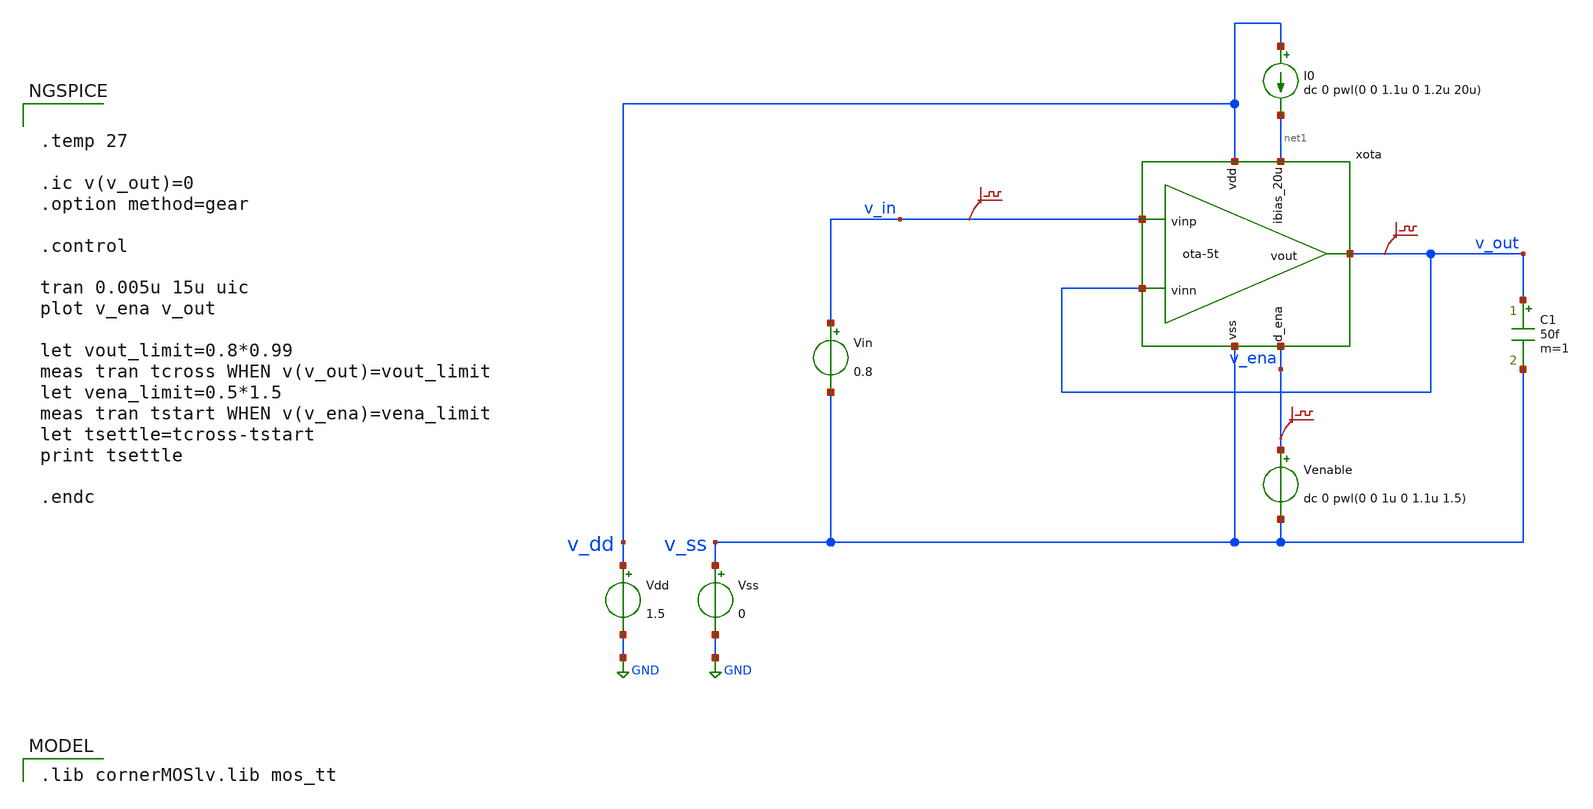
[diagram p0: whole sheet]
** sch_path: xschem/ota-5t_tb-tran.sch
* (c) 2024-2025 H. Pretl, Apache-2.0 license
**.subckt ota-5t_tb-tran
Vdd v_dd GND 1.5
xota v_dd v_out v_in v_out net1 v_ena v_ss ota-5t
Vss v_ss GND 0
C1 v_out v_ss 50f m=1
Vin v_in v_ss 0.8
I0 v_dd net1 dc 0 pwl(0 0 1.1u 0 1.2u 20u)
Venable v_ena v_ss dc 0 pwl(0 0 1u 0 1.1u 1.5)
.save v(v_in)
.save v(v_out)
.save v(v_ena)
**** begin user architecture code
 .lib cornerMOSlv.lib mos_tt



.temp 27

.ic v(v_out)=0
.option method=gear

.control

tran 0.005u 15u uic
plot v_ena v_out

let vout_limit=0.8*0.99
meas tran tcross WHEN v(v_out)=vout_limit
let vena_limit=0.5*1.5
meas tran tstart WHEN v(v_ena)=vena_limit
let tsettle=tcross-tstart
print tsettle

.endc


**** end user architecture code
**.ends
.GLOBAL GND
.end
